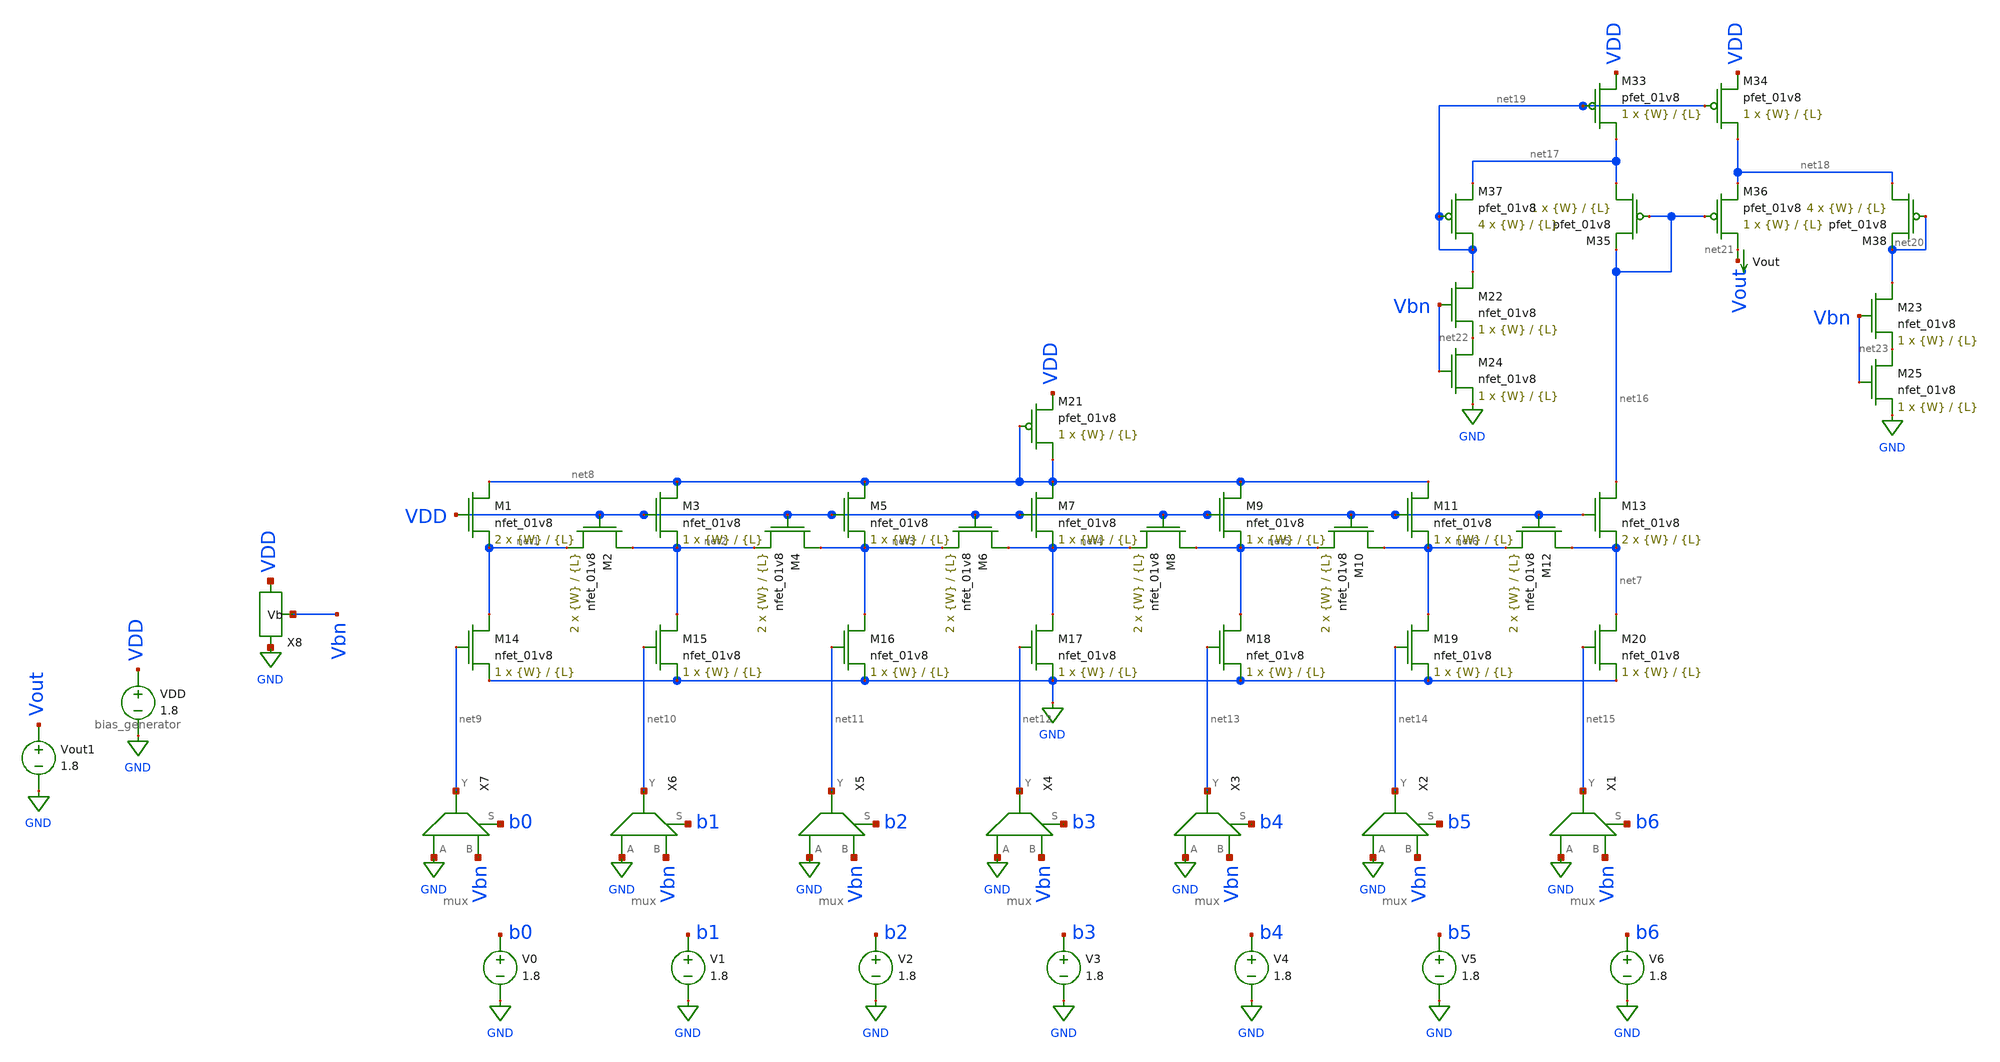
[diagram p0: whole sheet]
** sch_path: dac/schematics/misc/dac_output_current_current_mirror.sch
**.subckt dac_output_current_current_mirror
XM1 net8 VDD net1 GND sky130_fd_pr__nfet_01v8 L={L} W={W} nf=1 ad='int((nf+1)/2) * W/nf * 0.29' as='int((nf+2)/2) * W/nf * 0.29'
+ pd='2*int((nf+1)/2) * (W/nf + 0.29)' ps='2*int((nf+2)/2) * (W/nf + 0.29)' nrd='0.29 / W' nrs='0.29 / W'
+ sa=0 sb=0 sd=0 mult=2 m=2
XM2 net2 VDD net1 GND sky130_fd_pr__nfet_01v8 L={L} W={W} nf=1 ad='int((nf+1)/2) * W/nf * 0.29' as='int((nf+2)/2) * W/nf * 0.29'
+ pd='2*int((nf+1)/2) * (W/nf + 0.29)' ps='2*int((nf+2)/2) * (W/nf + 0.29)' nrd='0.29 / W' nrs='0.29 / W'
+ sa=0 sb=0 sd=0 mult=2 m=2
XM3 net8 VDD net2 GND sky130_fd_pr__nfet_01v8 L={L} W={W} nf=1 ad='int((nf+1)/2) * W/nf * 0.29' as='int((nf+2)/2) * W/nf * 0.29'
+ pd='2*int((nf+1)/2) * (W/nf + 0.29)' ps='2*int((nf+2)/2) * (W/nf + 0.29)' nrd='0.29 / W' nrs='0.29 / W'
+ sa=0 sb=0 sd=0 mult=1 m=1
XM4 net3 VDD net2 GND sky130_fd_pr__nfet_01v8 L={L} W={W} nf=1 ad='int((nf+1)/2) * W/nf * 0.29' as='int((nf+2)/2) * W/nf * 0.29'
+ pd='2*int((nf+1)/2) * (W/nf + 0.29)' ps='2*int((nf+2)/2) * (W/nf + 0.29)' nrd='0.29 / W' nrs='0.29 / W'
+ sa=0 sb=0 sd=0 mult=2 m=2
XM5 net8 VDD net3 GND sky130_fd_pr__nfet_01v8 L={L} W={W} nf=1 ad='int((nf+1)/2) * W/nf * 0.29' as='int((nf+2)/2) * W/nf * 0.29'
+ pd='2*int((nf+1)/2) * (W/nf + 0.29)' ps='2*int((nf+2)/2) * (W/nf + 0.29)' nrd='0.29 / W' nrs='0.29 / W'
+ sa=0 sb=0 sd=0 mult=1 m=1
XM6 net4 VDD net3 GND sky130_fd_pr__nfet_01v8 L={L} W={W} nf=1 ad='int((nf+1)/2) * W/nf * 0.29' as='int((nf+2)/2) * W/nf * 0.29'
+ pd='2*int((nf+1)/2) * (W/nf + 0.29)' ps='2*int((nf+2)/2) * (W/nf + 0.29)' nrd='0.29 / W' nrs='0.29 / W'
+ sa=0 sb=0 sd=0 mult=2 m=2
XM7 net8 VDD net4 GND sky130_fd_pr__nfet_01v8 L={L} W={W} nf=1 ad='int((nf+1)/2) * W/nf * 0.29' as='int((nf+2)/2) * W/nf * 0.29'
+ pd='2*int((nf+1)/2) * (W/nf + 0.29)' ps='2*int((nf+2)/2) * (W/nf + 0.29)' nrd='0.29 / W' nrs='0.29 / W'
+ sa=0 sb=0 sd=0 mult=1 m=1
XM8 net5 VDD net4 GND sky130_fd_pr__nfet_01v8 L={L} W={W} nf=1 ad='int((nf+1)/2) * W/nf * 0.29' as='int((nf+2)/2) * W/nf * 0.29'
+ pd='2*int((nf+1)/2) * (W/nf + 0.29)' ps='2*int((nf+2)/2) * (W/nf + 0.29)' nrd='0.29 / W' nrs='0.29 / W'
+ sa=0 sb=0 sd=0 mult=2 m=2
XM9 net8 VDD net5 GND sky130_fd_pr__nfet_01v8 L={L} W={W} nf=1 ad='int((nf+1)/2) * W/nf * 0.29' as='int((nf+2)/2) * W/nf * 0.29'
+ pd='2*int((nf+1)/2) * (W/nf + 0.29)' ps='2*int((nf+2)/2) * (W/nf + 0.29)' nrd='0.29 / W' nrs='0.29 / W'
+ sa=0 sb=0 sd=0 mult=1 m=1
XM10 net6 VDD net5 GND sky130_fd_pr__nfet_01v8 L={L} W={W} nf=1 ad='int((nf+1)/2) * W/nf * 0.29' as='int((nf+2)/2) * W/nf * 0.29'
+ pd='2*int((nf+1)/2) * (W/nf + 0.29)' ps='2*int((nf+2)/2) * (W/nf + 0.29)' nrd='0.29 / W' nrs='0.29 / W'
+ sa=0 sb=0 sd=0 mult=2 m=2
XM11 net8 VDD net6 GND sky130_fd_pr__nfet_01v8 L={L} W={W} nf=1 ad='int((nf+1)/2) * W/nf * 0.29' as='int((nf+2)/2) * W/nf * 0.29'
+ pd='2*int((nf+1)/2) * (W/nf + 0.29)' ps='2*int((nf+2)/2) * (W/nf + 0.29)' nrd='0.29 / W' nrs='0.29 / W'
+ sa=0 sb=0 sd=0 mult=1 m=1
XM12 net7 VDD net6 GND sky130_fd_pr__nfet_01v8 L={L} W={W} nf=1 ad='int((nf+1)/2) * W/nf * 0.29' as='int((nf+2)/2) * W/nf * 0.29'
+ pd='2*int((nf+1)/2) * (W/nf + 0.29)' ps='2*int((nf+2)/2) * (W/nf + 0.29)' nrd='0.29 / W' nrs='0.29 / W'
+ sa=0 sb=0 sd=0 mult=2 m=2
XM13 net16 VDD net7 GND sky130_fd_pr__nfet_01v8 L={L} W={W} nf=1 ad='int((nf+1)/2) * W/nf * 0.29' as='int((nf+2)/2) * W/nf * 0.29'
+ pd='2*int((nf+1)/2) * (W/nf + 0.29)' ps='2*int((nf+2)/2) * (W/nf + 0.29)' nrd='0.29 / W' nrs='0.29 / W'
+ sa=0 sb=0 sd=0 mult=2 m=2
XM14 net1 net9 GND GND sky130_fd_pr__nfet_01v8 L={L} W={W} nf=1 ad='int((nf+1)/2) * W/nf * 0.29' as='int((nf+2)/2) * W/nf * 0.29'
+ pd='2*int((nf+1)/2) * (W/nf + 0.29)' ps='2*int((nf+2)/2) * (W/nf + 0.29)' nrd='0.29 / W' nrs='0.29 / W'
+ sa=0 sb=0 sd=0 mult=1 m=1
XM15 net2 net10 GND GND sky130_fd_pr__nfet_01v8 L={L} W={W} nf=1 ad='int((nf+1)/2) * W/nf * 0.29' as='int((nf+2)/2) * W/nf * 0.29'
+ pd='2*int((nf+1)/2) * (W/nf + 0.29)' ps='2*int((nf+2)/2) * (W/nf + 0.29)' nrd='0.29 / W' nrs='0.29 / W'
+ sa=0 sb=0 sd=0 mult=1 m=1
XM16 net3 net11 GND GND sky130_fd_pr__nfet_01v8 L={L} W={W} nf=1 ad='int((nf+1)/2) * W/nf * 0.29' as='int((nf+2)/2) * W/nf * 0.29'
+ pd='2*int((nf+1)/2) * (W/nf + 0.29)' ps='2*int((nf+2)/2) * (W/nf + 0.29)' nrd='0.29 / W' nrs='0.29 / W'
+ sa=0 sb=0 sd=0 mult=1 m=1
XM17 net4 net12 GND GND sky130_fd_pr__nfet_01v8 L={L} W={W} nf=1 ad='int((nf+1)/2) * W/nf * 0.29' as='int((nf+2)/2) * W/nf * 0.29'
+ pd='2*int((nf+1)/2) * (W/nf + 0.29)' ps='2*int((nf+2)/2) * (W/nf + 0.29)' nrd='0.29 / W' nrs='0.29 / W'
+ sa=0 sb=0 sd=0 mult=1 m=1
XM18 net5 net13 GND GND sky130_fd_pr__nfet_01v8 L={L} W={W} nf=1 ad='int((nf+1)/2) * W/nf * 0.29' as='int((nf+2)/2) * W/nf * 0.29'
+ pd='2*int((nf+1)/2) * (W/nf + 0.29)' ps='2*int((nf+2)/2) * (W/nf + 0.29)' nrd='0.29 / W' nrs='0.29 / W'
+ sa=0 sb=0 sd=0 mult=1 m=1
XM19 net6 net14 GND GND sky130_fd_pr__nfet_01v8 L={L} W={W} nf=1 ad='int((nf+1)/2) * W/nf * 0.29' as='int((nf+2)/2) * W/nf * 0.29'
+ pd='2*int((nf+1)/2) * (W/nf + 0.29)' ps='2*int((nf+2)/2) * (W/nf + 0.29)' nrd='0.29 / W' nrs='0.29 / W'
+ sa=0 sb=0 sd=0 mult=1 m=1
XM20 net7 net15 GND GND sky130_fd_pr__nfet_01v8 L={L} W={W} nf=1 ad='int((nf+1)/2) * W/nf * 0.29' as='int((nf+2)/2) * W/nf * 0.29'
+ pd='2*int((nf+1)/2) * (W/nf + 0.29)' ps='2*int((nf+2)/2) * (W/nf + 0.29)' nrd='0.29 / W' nrs='0.29 / W'
+ sa=0 sb=0 sd=0 mult=1 m=1
X1 GND Vbn net15 b6 mux
X2 GND Vbn net14 b5 mux
X3 GND Vbn net13 b4 mux
X4 GND Vbn net12 b3 mux
X5 GND Vbn net11 b2 mux
X6 GND Vbn net10 b1 mux
X7 GND Vbn net9 b0 mux
V0 b0 GND 1.8
V1 b1 GND 1.8
V2 b2 GND 1.8
V3 b3 GND 1.8
V4 b4 GND 1.8
V5 b5 GND 1.8
V6 b6 GND 1.8
Vout net21 Vout 0
.save i(vout)
VDD VDD GND 1.8
X8 VDD GND Vbn bias_generator
XM33 net17 net19 VDD VDD sky130_fd_pr__pfet_01v8 L={L} W={W} nf=1 ad='int((nf+1)/2) * W/nf * 0.29' as='int((nf+2)/2) * W/nf * 0.29'
+ pd='2*int((nf+1)/2) * (W/nf + 0.29)' ps='2*int((nf+2)/2) * (W/nf + 0.29)' nrd='0.29 / W' nrs='0.29 / W'
+ sa=0 sb=0 sd=0 mult=1 m=1
XM34 net18 net19 VDD VDD sky130_fd_pr__pfet_01v8 L={L} W={W} nf=1 ad='int((nf+1)/2) * W/nf * 0.29' as='int((nf+2)/2) * W/nf * 0.29'
+ pd='2*int((nf+1)/2) * (W/nf + 0.29)' ps='2*int((nf+2)/2) * (W/nf + 0.29)' nrd='0.29 / W' nrs='0.29 / W'
+ sa=0 sb=0 sd=0 mult=1 m=1
XM35 net17 net16 net16 VDD sky130_fd_pr__pfet_01v8 L={L} W={W} nf=1 ad='int((nf+1)/2) * W/nf * 0.29'
+ as='int((nf+2)/2) * W/nf * 0.29' pd='2*int((nf+1)/2) * (W/nf + 0.29)' ps='2*int((nf+2)/2) * (W/nf + 0.29)'
+ nrd='0.29 / W' nrs='0.29 / W' sa=0 sb=0 sd=0 mult=1 m=1
XM36 net21 net16 net18 VDD sky130_fd_pr__pfet_01v8 L={L} W={W} nf=1 ad='int((nf+1)/2) * W/nf * 0.29'
+ as='int((nf+2)/2) * W/nf * 0.29' pd='2*int((nf+1)/2) * (W/nf + 0.29)' ps='2*int((nf+2)/2) * (W/nf + 0.29)'
+ nrd='0.29 / W' nrs='0.29 / W' sa=0 sb=0 sd=0 mult=1 m=1
XM37 net19 net19 net17 VDD sky130_fd_pr__pfet_01v8 L={L} W={W} nf=1 ad='int((nf+1)/2) * W/nf * 0.29'
+ as='int((nf+2)/2) * W/nf * 0.29' pd='2*int((nf+1)/2) * (W/nf + 0.29)' ps='2*int((nf+2)/2) * (W/nf + 0.29)'
+ nrd='0.29 / W' nrs='0.29 / W' sa=0 sb=0 sd=0 mult=4 m=4
XM38 net18 net20 net20 VDD sky130_fd_pr__pfet_01v8 L={L} W={W} nf=1 ad='int((nf+1)/2) * W/nf * 0.29'
+ as='int((nf+2)/2) * W/nf * 0.29' pd='2*int((nf+1)/2) * (W/nf + 0.29)' ps='2*int((nf+2)/2) * (W/nf + 0.29)'
+ nrd='0.29 / W' nrs='0.29 / W' sa=0 sb=0 sd=0 mult=4 m=4
XM21 net8 net8 VDD VDD sky130_fd_pr__pfet_01v8 L={L} W={W} nf=1 ad='int((nf+1)/2) * W/nf * 0.29' as='int((nf+2)/2) * W/nf * 0.29'
+ pd='2*int((nf+1)/2) * (W/nf + 0.29)' ps='2*int((nf+2)/2) * (W/nf + 0.29)' nrd='0.29 / W' nrs='0.29 / W'
+ sa=0 sb=0 sd=0 mult=1 m=1
Vout1 Vout GND 1.8
XM22 net19 Vbn net22 GND sky130_fd_pr__nfet_01v8 L={L} W={W} nf=1 ad='int((nf+1)/2) * W/nf * 0.29' as='int((nf+2)/2) * W/nf * 0.29'
+ pd='2*int((nf+1)/2) * (W/nf + 0.29)' ps='2*int((nf+2)/2) * (W/nf + 0.29)' nrd='0.29 / W' nrs='0.29 / W'
+ sa=0 sb=0 sd=0 mult=1 m=1
XM23 net20 Vbn net23 GND sky130_fd_pr__nfet_01v8 L={L} W={W} nf=1 ad='int((nf+1)/2) * W/nf * 0.29' as='int((nf+2)/2) * W/nf * 0.29'
+ pd='2*int((nf+1)/2) * (W/nf + 0.29)' ps='2*int((nf+2)/2) * (W/nf + 0.29)' nrd='0.29 / W' nrs='0.29 / W'
+ sa=0 sb=0 sd=0 mult=1 m=1
XM24 net22 Vbn GND GND sky130_fd_pr__nfet_01v8 L={L} W={W} nf=1 ad='int((nf+1)/2) * W/nf * 0.29' as='int((nf+2)/2) * W/nf * 0.29'
+ pd='2*int((nf+1)/2) * (W/nf + 0.29)' ps='2*int((nf+2)/2) * (W/nf + 0.29)' nrd='0.29 / W' nrs='0.29 / W'
+ sa=0 sb=0 sd=0 mult=1 m=1
XM25 net23 Vbn GND GND sky130_fd_pr__nfet_01v8 L={L} W={W} nf=1 ad='int((nf+1)/2) * W/nf * 0.29' as='int((nf+2)/2) * W/nf * 0.29'
+ pd='2*int((nf+1)/2) * (W/nf + 0.29)' ps='2*int((nf+2)/2) * (W/nf + 0.29)' nrd='0.29 / W' nrs='0.29 / W'
+ sa=0 sb=0 sd=0 mult=1 m=1
**** begin user architecture code

.param W=1
.param L=0.5
.dc Vout1 0 1.8 0.01
.save v(Vout) i(Vout) v(VDD) v(Vbn)


.option wnflag=1
.param MC_SWITCH=0.0
.lib ~/skywater/skywater-pdk/libraries/sky130_fd_pr_ngspice/latest/models/sky130.lib.spice tt

**** end user architecture code
**.ends

* expanding   symbol:  /home/madvlsi/Documents/current-output-dac-vlsi/schematics/mux.sym # of
*+ pins=4
** sym_path: dac/schematics/mux.sym
** sch_path: dac/schematics/mux.sch
.subckt mux A B Y S
*.ipin A
*.ipin B
*.ipin S
*.opin Y
XM1 A S Y VDD sky130_fd_pr__pfet_01v8 L=0.15 W=1 nf=1 ad='int((nf+1)/2) * W/nf * 0.29' as='int((nf+2)/2) * W/nf * 0.29'
+ pd='2*int((nf+1)/2) * (W/nf + 0.29)' ps='2*int((nf+2)/2) * (W/nf + 0.29)' nrd='0.29 / W' nrs='0.29 / W'
+ sa=0 sb=0 sd=0 mult=1 m=1
XM3 net1 S VDD VDD sky130_fd_pr__pfet_01v8 L=0.15 W=1 nf=1 ad='int((nf+1)/2) * W/nf * 0.29' as='int((nf+2)/2) * W/nf * 0.29'
+ pd='2*int((nf+1)/2) * (W/nf + 0.29)' ps='2*int((nf+2)/2) * (W/nf + 0.29)' nrd='0.29 / W' nrs='0.29 / W'
+ sa=0 sb=0 sd=0 mult=1 m=1
XM4 net1 S GND GND sky130_fd_pr__nfet_01v8 L=0.15 W=1 nf=1 ad='int((nf+1)/2) * W/nf * 0.29' as='int((nf+2)/2) * W/nf * 0.29'
+ pd='2*int((nf+1)/2) * (W/nf + 0.29)' ps='2*int((nf+2)/2) * (W/nf + 0.29)' nrd='0.29 / W' nrs='0.29 / W'
+ sa=0 sb=0 sd=0 mult=1 m=1
XM5 A net1 Y GND sky130_fd_pr__nfet_01v8 L=0.15 W=1 nf=1 ad='int((nf+1)/2) * W/nf * 0.29' as='int((nf+2)/2) * W/nf * 0.29'
+ pd='2*int((nf+1)/2) * (W/nf + 0.29)' ps='2*int((nf+2)/2) * (W/nf + 0.29)' nrd='0.29 / W' nrs='0.29 / W'
+ sa=0 sb=0 sd=0 mult=1 m=1
XM2 B net1 Y VDD sky130_fd_pr__pfet_01v8 L=0.15 W=1 nf=1 ad='int((nf+1)/2) * W/nf * 0.29' as='int((nf+2)/2) * W/nf * 0.29'
+ pd='2*int((nf+1)/2) * (W/nf + 0.29)' ps='2*int((nf+2)/2) * (W/nf + 0.29)' nrd='0.29 / W' nrs='0.29 / W'
+ sa=0 sb=0 sd=0 mult=1 m=1
XM6 B S Y GND sky130_fd_pr__nfet_01v8 L=0.15 W=1 nf=1 ad='int((nf+1)/2) * W/nf * 0.29' as='int((nf+2)/2) * W/nf * 0.29'
+ pd='2*int((nf+1)/2) * (W/nf + 0.29)' ps='2*int((nf+2)/2) * (W/nf + 0.29)' nrd='0.29 / W' nrs='0.29 / W'
+ sa=0 sb=0 sd=0 mult=1 m=1
.ends


* expanding   symbol:  /home/madvlsi/Documents/current-output-dac-vlsi/schematics/bias_generator.sym
*+ # of pins=3
** sym_path: dac/schematics/bias_generator.sym
** sch_path: dac/schematics/bias_generator.sch
.subckt bias_generator VP VN Vb
*.iopin VP
*.iopin VN
*.opin Vb
XM20 VP net2 net3 VDD sky130_fd_pr__pfet_01v8 L=0.5 W=1 nf=1 ad='int((nf+1)/2) * W/nf * 0.29' as='int((nf+2)/2) * W/nf * 0.29'
+ pd='2*int((nf+1)/2) * (W/nf + 0.29)' ps='2*int((nf+2)/2) * (W/nf + 0.29)' nrd='0.29 / W' nrs='0.29 / W'
+ sa=0 sb=0 sd=0 mult=1 m=1
XM21 net4 net3 net3 GND sky130_fd_pr__nfet_01v8 L=0.5 W=1 nf=1 ad='int((nf+1)/2) * W/nf * 0.29' as='int((nf+2)/2) * W/nf * 0.29'
+ pd='2*int((nf+1)/2) * (W/nf + 0.29)' ps='2*int((nf+2)/2) * (W/nf + 0.29)' nrd='0.29 / W' nrs='0.29 / W'
+ sa=0 sb=0 sd=0 mult=8 m=8
R3 net4 VN 400k m=1
XM22 net1 net3 VN GND sky130_fd_pr__nfet_01v8 L=0.5 W=1 nf=1 ad='int((nf+1)/2) * W/nf * 0.29' as='int((nf+2)/2) * W/nf * 0.29'
+ pd='2*int((nf+1)/2) * (W/nf + 0.29)' ps='2*int((nf+2)/2) * (W/nf + 0.29)' nrd='0.29 / W' nrs='0.29 / W'
+ sa=0 sb=0 sd=0 mult=1 m=1
XM23 VN Vb net2 GND sky130_fd_pr__nfet_01v8 L=0.5 W=1 nf=1 ad='int((nf+1)/2) * W/nf * 0.29' as='int((nf+2)/2) * W/nf * 0.29'
+ pd='2*int((nf+1)/2) * (W/nf + 0.29)' ps='2*int((nf+2)/2) * (W/nf + 0.29)' nrd='0.29 / W' nrs='0.29 / W'
+ sa=0 sb=0 sd=0 mult=1 m=1
XM24 Vb Vb VN GND sky130_fd_pr__nfet_01v8 L=0.5 W=1 nf=1 ad='int((nf+1)/2) * W/nf * 0.29' as='int((nf+2)/2) * W/nf * 0.29'
+ pd='2*int((nf+1)/2) * (W/nf + 0.29)' ps='2*int((nf+2)/2) * (W/nf + 0.29)' nrd='0.29 / W' nrs='0.29 / W'
+ sa=0 sb=0 sd=0 mult=1 m=1
XM25 VP net1 net1 VDD sky130_fd_pr__pfet_01v8 L=0.5 W=1 nf=1 ad='int((nf+1)/2) * W/nf * 0.29' as='int((nf+2)/2) * W/nf * 0.29'
+ pd='2*int((nf+1)/2) * (W/nf + 0.29)' ps='2*int((nf+2)/2) * (W/nf + 0.29)' nrd='0.29 / W' nrs='0.29 / W'
+ sa=0 sb=0 sd=0 mult=1 m=1
XM26 net2 net1 VP VDD sky130_fd_pr__pfet_01v8 L=0.5 W=1 nf=1 ad='int((nf+1)/2) * W/nf * 0.29' as='int((nf+2)/2) * W/nf * 0.29'
+ pd='2*int((nf+1)/2) * (W/nf + 0.29)' ps='2*int((nf+2)/2) * (W/nf + 0.29)' nrd='0.29 / W' nrs='0.29 / W'
+ sa=0 sb=0 sd=0 mult=1 m=1
XM27 Vb net2 VP VDD sky130_fd_pr__pfet_01v8 L=0.5 W=1 nf=1 ad='int((nf+1)/2) * W/nf * 0.29' as='int((nf+2)/2) * W/nf * 0.29'
+ pd='2*int((nf+1)/2) * (W/nf + 0.29)' ps='2*int((nf+2)/2) * (W/nf + 0.29)' nrd='0.29 / W' nrs='0.29 / W'
+ sa=0 sb=0 sd=0 mult=1 m=1
.ends

.GLOBAL GND
.GLOBAL VDD
.end
